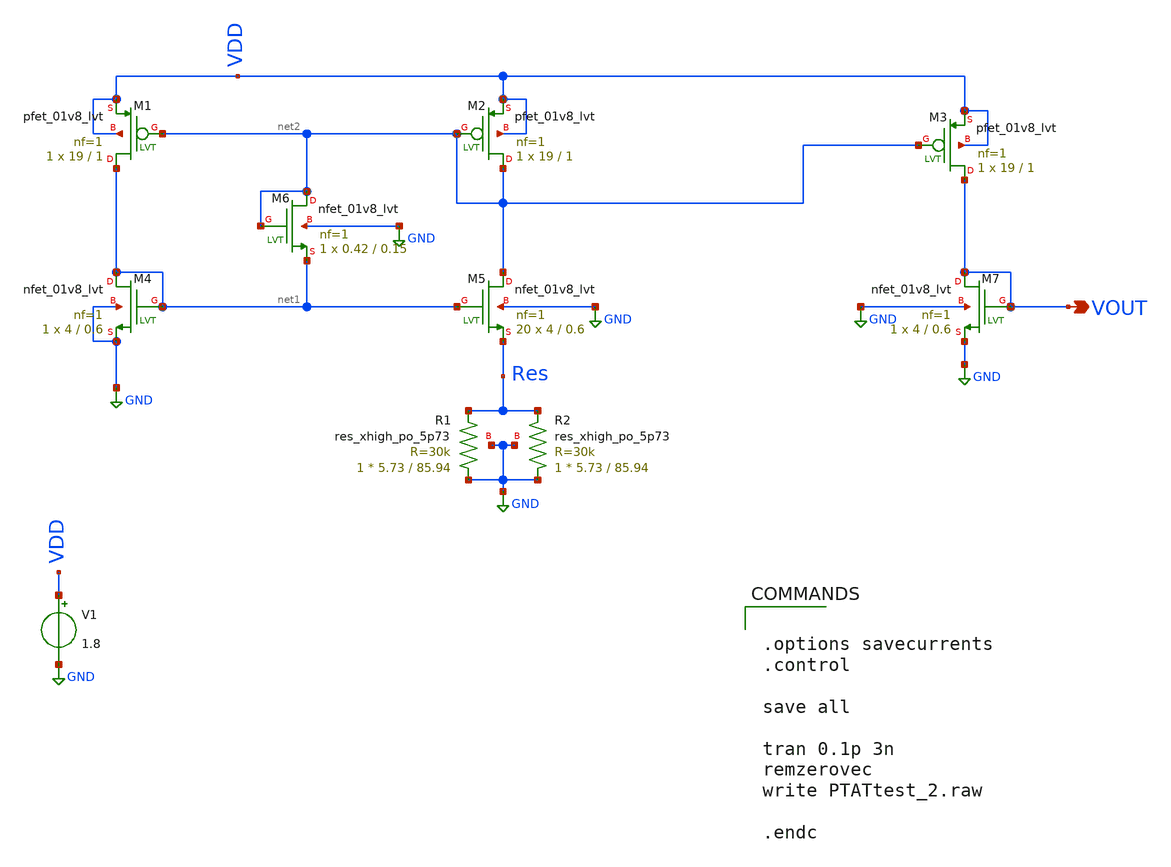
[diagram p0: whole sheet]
** sch_path: PTAT/xschem/PTATtest_2.sch
.lib $::SKYWATER_MODELS/sky130.lib.spice tt
.include $::SKYWATER_STDCELLS/sky130_fd_sc_hd.spice

**.subckt PTATtest_2 VOUT
*.opin VOUT
V1 VDD GND 1.8
XM1 net1 net2 VDD VDD sky130_fd_pr__pfet_01v8_lvt L=1 W=19 nf=1 ad='int((nf+1)/2) * W/nf * 0.29' as='int((nf+2)/2) * W/nf * 0.29'
+ pd='2*int((nf+1)/2) * (W/nf + 0.29)' ps='2*int((nf+2)/2) * (W/nf + 0.29)' nrd='0.29 / W' nrs='0.29 / W'
+ sa=0 sb=0 sd=0 mult=1 m=1
XM2 net2 net2 VDD VDD sky130_fd_pr__pfet_01v8_lvt L=1 W=19 nf=1 ad='int((nf+1)/2) * W/nf * 0.29' as='int((nf+2)/2) * W/nf * 0.29'
+ pd='2*int((nf+1)/2) * (W/nf + 0.29)' ps='2*int((nf+2)/2) * (W/nf + 0.29)' nrd='0.29 / W' nrs='0.29 / W'
+ sa=0 sb=0 sd=0 mult=1 m=1
XM3 VOUT net2 VDD VDD sky130_fd_pr__pfet_01v8_lvt L=1 W=19 nf=1 ad='int((nf+1)/2) * W/nf * 0.29' as='int((nf+2)/2) * W/nf * 0.29'
+ pd='2*int((nf+1)/2) * (W/nf + 0.29)' ps='2*int((nf+2)/2) * (W/nf + 0.29)' nrd='0.29 / W' nrs='0.29 / W'
+ sa=0 sb=0 sd=0 mult=1 m=1
XM4 net1 net1 GND GND sky130_fd_pr__nfet_01v8_lvt L=0.6 W=4 nf=1 ad='int((nf+1)/2) * W/nf * 0.29' as='int((nf+2)/2) * W/nf * 0.29'
+ pd='2*int((nf+1)/2) * (W/nf + 0.29)' ps='2*int((nf+2)/2) * (W/nf + 0.29)' nrd='0.29 / W' nrs='0.29 / W'
+ sa=0 sb=0 sd=0 mult=1 m=1
XM5 net2 net1 Res GND sky130_fd_pr__nfet_01v8_lvt L=0.6 W=4 nf=1 ad='int((nf+1)/2) * W/nf * 0.29' as='int((nf+2)/2) * W/nf * 0.29'
+ pd='2*int((nf+1)/2) * (W/nf + 0.29)' ps='2*int((nf+2)/2) * (W/nf + 0.29)' nrd='0.29 / W' nrs='0.29 / W'
+ sa=0 sb=0 sd=0 mult=20 m=20
XM6 net2 net2 net1 GND sky130_fd_pr__nfet_01v8_lvt L=0.15 W=0.42 nf=1 ad='int((nf+1)/2) * W/nf * 0.29'
+ as='int((nf+2)/2) * W/nf * 0.29' pd='2*int((nf+1)/2) * (W/nf + 0.29)' ps='2*int((nf+2)/2) * (W/nf + 0.29)'
+ nrd='0.29 / W' nrs='0.29 / W' sa=0 sb=0 sd=0 mult=1 m=1
XM7 VOUT VOUT GND GND sky130_fd_pr__nfet_01v8_lvt L=0.6 W=4 nf=1 ad='int((nf+1)/2) * W/nf * 0.29' as='int((nf+2)/2) * W/nf * 0.29'
+ pd='2*int((nf+1)/2) * (W/nf + 0.29)' ps='2*int((nf+2)/2) * (W/nf + 0.29)' nrd='0.29 / W' nrs='0.29 / W'
+ sa=0 sb=0 sd=0 mult=1 m=1
XR1 GND Res GND sky130_fd_pr__res_xhigh_po_5p73 L=85.94 mult=1 m=1
XR2 GND Res GND sky130_fd_pr__res_xhigh_po_5p73 L=85.94 mult=1 m=1
**** begin user architecture code


.options savecurrents
.control

save all

tran 0.1p 3n
remzerovec
write PTATtest_2.raw

.endc


**** end user architecture code
**.ends
.GLOBAL GND
.end
